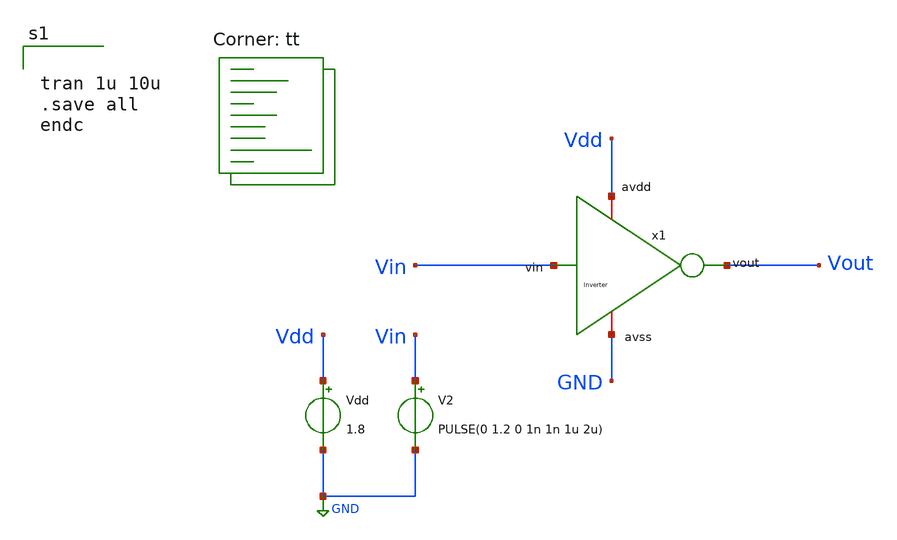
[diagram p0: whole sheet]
** sch_path: XSCHEM_DESIGNS/InvTest.sch
**.subckt InvTest
x1 Vdd Vin Vout GND Inverter
Vdd Vdd GND 1.8
V2 Vin GND PULSE(0 1.2 0 1n 1n 1u 2u)
**** begin user architecture code
.lib $::SKYWATER_MODELS/sky130.lib.spice tt


tran 1u 10u
.save all
endc


**** end user architecture code
**.ends

* expanding   symbol:  Inverter.sym # of pins=4
** sym_path: XSCHEM_DESIGNS/Inverter.sym
** sch_path: XSCHEM_DESIGNS/Inverter.sch
.subckt Inverter avdd vin vout avss
*.ipin vin
*.opin vout
*.iopin avdd
*.iopin avss
XM1 vout vin avdd avdd sky130_fd_pr__pfet_01v8 L=0.3 W=1.7 nf=1 ad='int((1 + 1)/2) * 1.7 / 1 * 0.29'
+ as='int((1 + 2)/2) * 1.7 / 1 * 0.29' pd='2*int((1 + 1)/2) * (1.7 / 1 + 0.29)' ps='2*int((1 + 2)/2) * (1.7 / 1 + 0.29)'
+ nrd='0.29 / 1.7 ' nrs='0.29 / 1.7 ' sa=0 sb=0 sd=0 mult=1 m=1
XM2 vout vin avss avss sky130_fd_pr__nfet_01v8 L=0.3 W=0.85 nf=1 ad='int((1 + 1)/2) * 0.85 / 1 * 0.29'
+ as='int((1 + 2)/2) * 0.85 / 1 * 0.29' pd='2*int((1 + 1)/2) * (0.85 / 1 + 0.29)' ps='2*int((1 + 2)/2) * (0.85 / 1 + 0.29)'
+ nrd='0.29 / 0.85 ' nrs='0.29 / 0.85 ' sa=0 sb=0 sd=0 mult=1 m=1
.ends

.GLOBAL GND
.end
